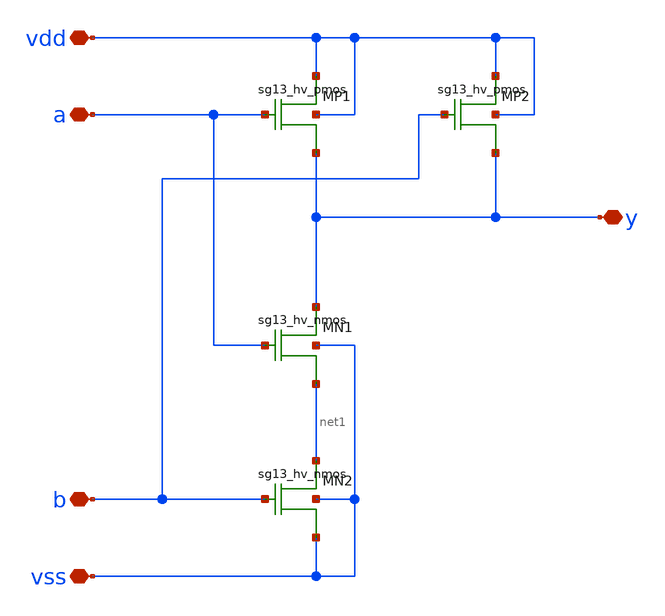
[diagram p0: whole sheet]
** sch_path: xschem/logic_gates/NANDHV.sch
**.subckt NANDHV vdd vss y a b
*.iopin vdd
*.iopin vss
*.iopin y
*.iopin a
*.iopin b
XMP1 vdd a y vdd sg13_hv_pmos w=2.0u l=0.45u ng=1 m=1
XMP2 vdd b y vdd sg13_hv_pmos w=2.0u l=0.45u ng=1 m=1
XMN1 y a net1 vss sg13_hv_nmos w=2.0u l=0.45u ng=1 m=1
XMN2 net1 b vss vss sg13_hv_nmos w=2.0u l=0.45u ng=1 m=1
**.ends
.end
